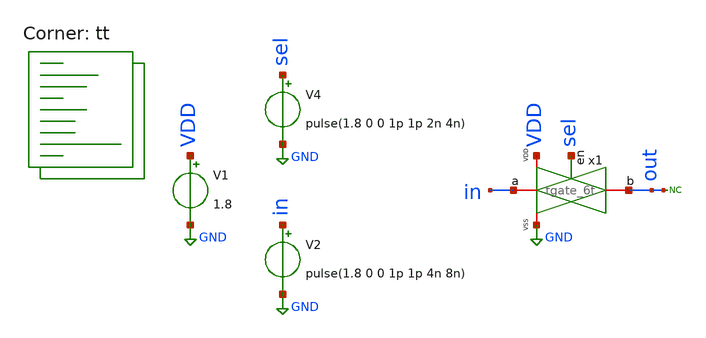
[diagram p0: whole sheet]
** sch_path: xsch/tb/tgate/6t/tgate_6t_tran.sch
**.subckt tgate_6t_tran
V1 VDD GND 1.8
V2 in GND pulse(1.8 0 0 1p 1p 4n 8n)
V4 sel GND pulse(1.8 0 0 1p 1p 2n 4n)
* noconn out
x1 VDD GND in out sel tgate_6t
**** begin user architecture code
.lib $::SKYWATER_MODELS/sky130.lib.spice tt



.control
save v(in) v(out) v(sel) v(selb)
tran 1p 10n
write tgate_6t_tran.raw
quit
.endc


**** end user architecture code
**.ends

* expanding   symbol:  ip/tgate/tgate_6t.sym # of pins=5
** sym_path: xsch/ip/tgate/tgate_6t.sym
** sch_path: xsch/ip/tgate/tgate_6t.sch
.subckt tgate_6t VDD VSS a b en
*.iopin a
*.iopin b
*.ipin en
*.iopin VDD
*.iopin VSS
XM2 selb en VSS VSS sky130_fd_pr__nfet_01v8 L=0.15 W=1 nf=1 ad='int((1 + 1)/2) * 1 / 1 * 0.29' as='int((1 + 2)/2) * 1 / 1 * 0.29'
+ pd='2*int((1 + 1)/2) * (1 / 1 + 0.29)' ps='2*int((1 + 2)/2) * (1 / 1 + 0.29)' nrd='0.29 / 1 ' nrs='0.29 / 1 '
+ sa=0 sb=0 sd=0 mult=1 m=1
XM11 selb en VDD VDD sky130_fd_pr__pfet_01v8 L=0.15 W=2 nf=1 ad='int((nf+1)/2) * W/nf * 0.29' as='int((nf+2)/2) * W/nf * 0.29'
+ pd='2*int((nf+1)/2) * (W/nf + 0.29)' ps='2*int((nf+2)/2) * (W/nf + 0.29)' nrd='0.29 / W' nrs='0.29 / W'
+ sa=0 sb=0 sd=0 mult=1 m=1
XM1 sel selb VSS VSS sky130_fd_pr__nfet_01v8 L=0.15 W=1 nf=1 ad='int((1 + 1)/2) * 1 / 1 * 0.29' as='int((1 + 2)/2) * 1 / 1 * 0.29'
+ pd='2*int((1 + 1)/2) * (1 / 1 + 0.29)' ps='2*int((1 + 2)/2) * (1 / 1 + 0.29)' nrd='0.29 / 1 ' nrs='0.29 / 1 '
+ sa=0 sb=0 sd=0 mult=1 m=1
XM3 sel selb VDD VDD sky130_fd_pr__pfet_01v8 L=0.15 W=2 nf=1 ad='int((nf+1)/2) * W/nf * 0.29' as='int((nf+2)/2) * W/nf * 0.29'
+ pd='2*int((nf+1)/2) * (W/nf + 0.29)' ps='2*int((nf+2)/2) * (W/nf + 0.29)' nrd='0.29 / W' nrs='0.29 / W'
+ sa=0 sb=0 sd=0 mult=1 m=1
XM4 a selb b VDD sky130_fd_pr__pfet_01v8 L=0.15 W=2 nf=1 ad='int((nf+1)/2) * W/nf * 0.29' as='int((nf+2)/2) * W/nf * 0.29'
+ pd='2*int((nf+1)/2) * (W/nf + 0.29)' ps='2*int((nf+2)/2) * (W/nf + 0.29)' nrd='0.29 / W' nrs='0.29 / W'
+ sa=0 sb=0 sd=0 mult=1 m=1
XM5 a sel b VSS sky130_fd_pr__nfet_01v8 L=0.15 W=1 nf=1 ad='int((1 + 1)/2) * 1 / 1 * 0.29' as='int((1 + 2)/2) * 1 / 1 * 0.29'
+ pd='2*int((1 + 1)/2) * (1 / 1 + 0.29)' ps='2*int((1 + 2)/2) * (1 / 1 + 0.29)' nrd='0.29 / 1 ' nrs='0.29 / 1 '
+ sa=0 sb=0 sd=0 mult=1 m=1
.ends

.GLOBAL GND
.end
